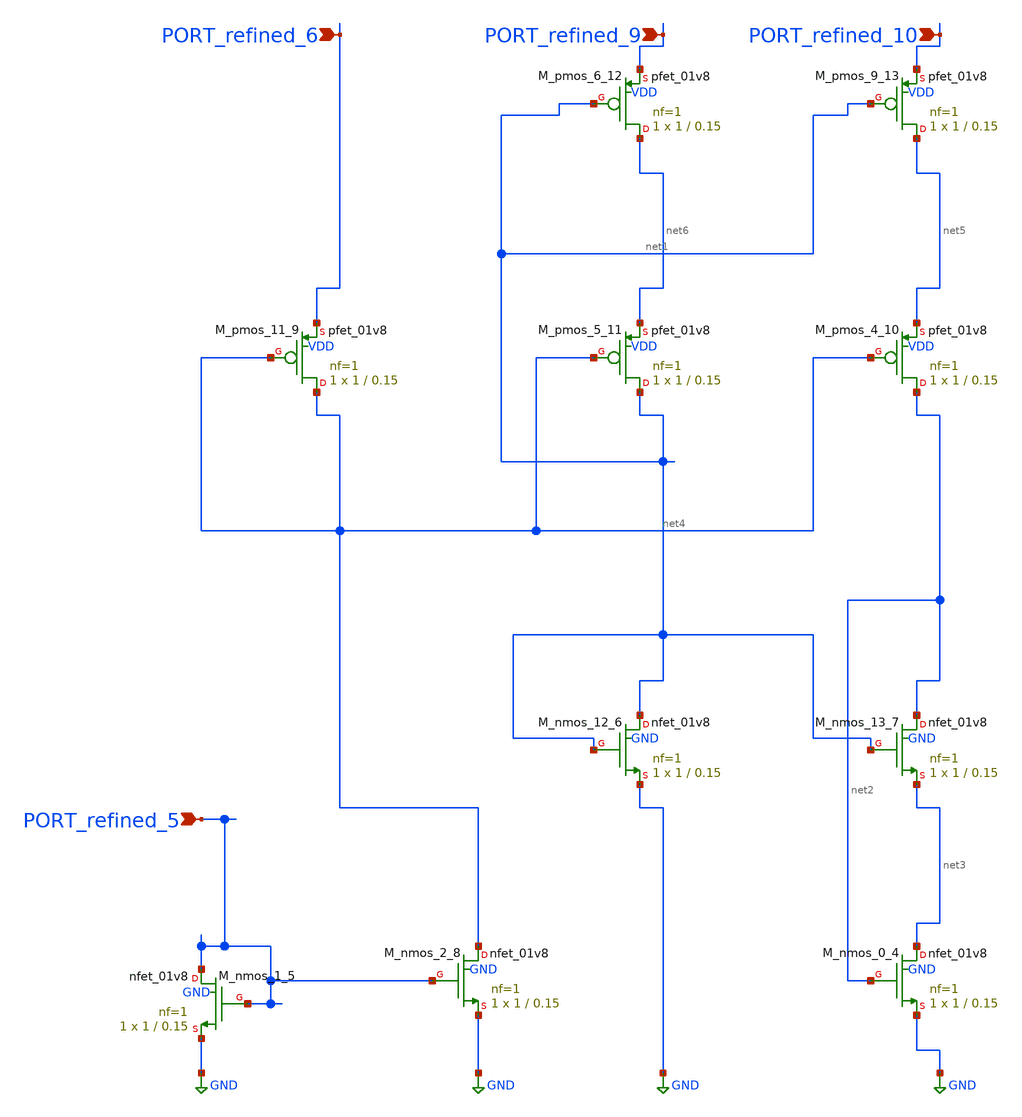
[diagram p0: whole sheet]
** sch_path: schematics/p07_fig9_bias.sch
**.subckt p07_fig9_bias PORT_refined_9 PORT_refined_10 PORT_refined_6 PORT_refined_5
*.ipin PORT_refined_9
*.ipin PORT_refined_10
*.ipin PORT_refined_6
*.ipin PORT_refined_5
XM_nmos_0_4 net3 net2 GND GND sky130_fd_pr__nfet_01v8 L=0.15 W=1 nf=1 ad='int((1 + 1)/2) * 1 / 1 * 0.29'
+ as='int((1 + 2)/2) * 1 / 1 * 0.29' pd='2*int((1 + 1)/2) * (1 / 1 + 0.29)' ps='2*int((1 + 2)/2) * (1 / 1 + 0.29)'
+ nrd='0.29 / 1 ' nrs='0.29 / 1 ' sa=0 sb=0 sd=0 mult=1 m=1
XM_nmos_1_5 PORT_refined_5 PORT_refined_5 GND GND sky130_fd_pr__nfet_01v8 L=0.15 W=1 nf=1 ad='int((1 + 1)/2) * 1 / 1 * 0.29'
+ as='int((1 + 2)/2) * 1 / 1 * 0.29' pd='2*int((1 + 1)/2) * (1 / 1 + 0.29)' ps='2*int((1 + 2)/2) * (1 / 1 + 0.29)'
+ nrd='0.29 / 1 ' nrs='0.29 / 1 ' sa=0 sb=0 sd=0 mult=1 m=1
XM_nmos_12_6 net1 net1 GND GND sky130_fd_pr__nfet_01v8 L=0.15 W=1 nf=1 ad='int((1 + 1)/2) * 1 / 1 * 0.29'
+ as='int((1 + 2)/2) * 1 / 1 * 0.29' pd='2*int((1 + 1)/2) * (1 / 1 + 0.29)' ps='2*int((1 + 2)/2) * (1 / 1 + 0.29)'
+ nrd='0.29 / 1 ' nrs='0.29 / 1 ' sa=0 sb=0 sd=0 mult=1 m=1
XM_nmos_13_7 net2 net1 net3 GND sky130_fd_pr__nfet_01v8 L=0.15 W=1 nf=1 ad='int((1 + 1)/2) * 1 / 1 * 0.29'
+ as='int((1 + 2)/2) * 1 / 1 * 0.29' pd='2*int((1 + 1)/2) * (1 / 1 + 0.29)' ps='2*int((1 + 2)/2) * (1 / 1 + 0.29)'
+ nrd='0.29 / 1 ' nrs='0.29 / 1 ' sa=0 sb=0 sd=0 mult=1 m=1
XM_nmos_2_8 net4 PORT_refined_5 GND GND sky130_fd_pr__nfet_01v8 L=0.15 W=1 nf=1 ad='int((1 + 1)/2) * 1 / 1 * 0.29'
+ as='int((1 + 2)/2) * 1 / 1 * 0.29' pd='2*int((1 + 1)/2) * (1 / 1 + 0.29)' ps='2*int((1 + 2)/2) * (1 / 1 + 0.29)'
+ nrd='0.29 / 1 ' nrs='0.29 / 1 ' sa=0 sb=0 sd=0 mult=1 m=1
XM_pmos_11_9 net4 net4 PORT_refined_6 VDD sky130_fd_pr__pfet_01v8 L=0.15 W=1 nf=1 ad='int((1 + 1)/2) * 1 / 1 * 0.29'
+ as='int((1 + 2)/2) * 1 / 1 * 0.29' pd='2*int((1 + 1)/2) * (1 / 1 + 0.29)' ps='2*int((1 + 2)/2) * (1 / 1 + 0.29)'
+ nrd='0.29 / 1 ' nrs='0.29 / 1 ' sa=0 sb=0 sd=0 mult=1 m=1
XM_pmos_4_10 net2 net4 net5 VDD sky130_fd_pr__pfet_01v8 L=0.15 W=1 nf=1 ad='int((1 + 1)/2) * 1 / 1 * 0.29'
+ as='int((1 + 2)/2) * 1 / 1 * 0.29' pd='2*int((1 + 1)/2) * (1 / 1 + 0.29)' ps='2*int((1 + 2)/2) * (1 / 1 + 0.29)'
+ nrd='0.29 / 1 ' nrs='0.29 / 1 ' sa=0 sb=0 sd=0 mult=1 m=1
XM_pmos_5_11 net1 net4 net6 VDD sky130_fd_pr__pfet_01v8 L=0.15 W=1 nf=1 ad='int((1 + 1)/2) * 1 / 1 * 0.29'
+ as='int((1 + 2)/2) * 1 / 1 * 0.29' pd='2*int((1 + 1)/2) * (1 / 1 + 0.29)' ps='2*int((1 + 2)/2) * (1 / 1 + 0.29)'
+ nrd='0.29 / 1 ' nrs='0.29 / 1 ' sa=0 sb=0 sd=0 mult=1 m=1
XM_pmos_6_12 net6 net1 PORT_refined_9 VDD sky130_fd_pr__pfet_01v8 L=0.15 W=1 nf=1 ad='int((1 + 1)/2) * 1 / 1 * 0.29'
+ as='int((1 + 2)/2) * 1 / 1 * 0.29' pd='2*int((1 + 1)/2) * (1 / 1 + 0.29)' ps='2*int((1 + 2)/2) * (1 / 1 + 0.29)'
+ nrd='0.29 / 1 ' nrs='0.29 / 1 ' sa=0 sb=0 sd=0 mult=1 m=1
XM_pmos_9_13 net5 net1 PORT_refined_10 VDD sky130_fd_pr__pfet_01v8 L=0.15 W=1 nf=1 ad='int((1 + 1)/2) * 1 / 1 * 0.29'
+ as='int((1 + 2)/2) * 1 / 1 * 0.29' pd='2*int((1 + 1)/2) * (1 / 1 + 0.29)' ps='2*int((1 + 2)/2) * (1 / 1 + 0.29)'
+ nrd='0.29 / 1 ' nrs='0.29 / 1 ' sa=0 sb=0 sd=0 mult=1 m=1
**.ends
.GLOBAL GND
.end
